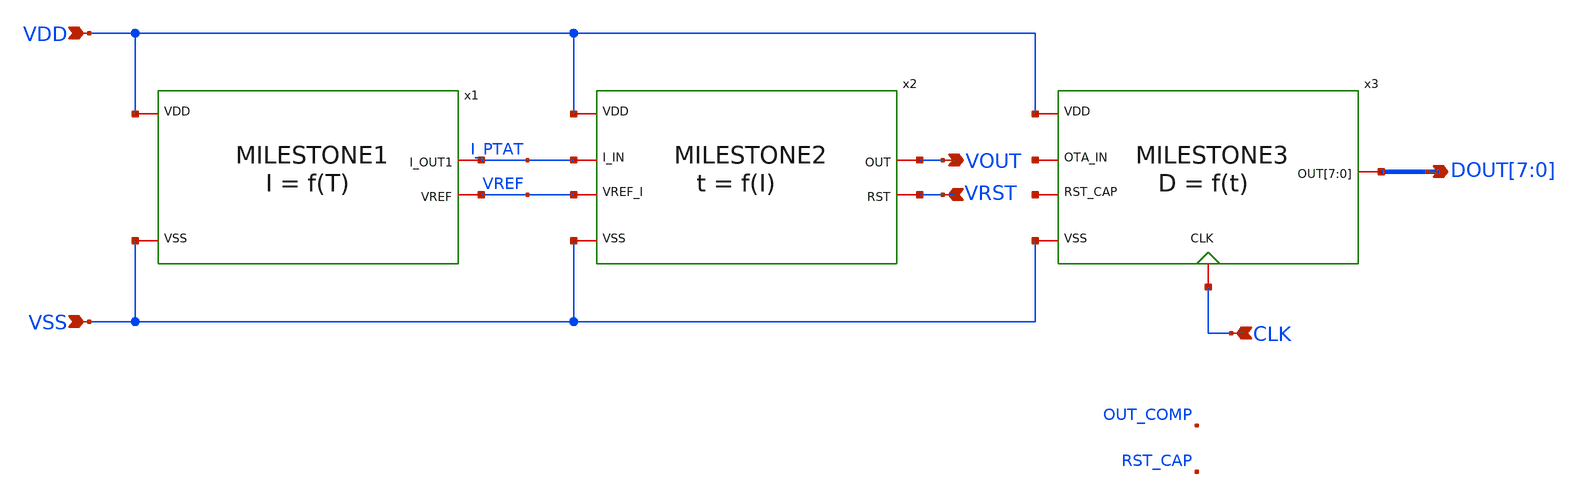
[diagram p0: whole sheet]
** sch_path: design/CNR_GR03_SKY130NM/TOPLEVEL.sch
**.subckt TOPLEVEL VDD VSS CLK DOUT[7],DOUT[6],DOUT[5],DOUT[4],DOUT[3],DOUT[2],DOUT[1],DOUT[0] VRST
*+ VOUT
*.ipin VDD
*.ipin VSS
*.ipin CLK
*.opin DOUT[7],DOUT[6],DOUT[5],DOUT[4],DOUT[3],DOUT[2],DOUT[1],DOUT[0]
*.ipin VRST
*.opin VOUT
x1 VDD I_PTAT VREF VSS MILESTONE1
x2 I_PTAT VREF VOUT VDD VRST VSS MILESTONE2
x3 net1 net2 CLK DOUT[7] DOUT[6] DOUT[5] DOUT[4] DOUT[3] DOUT[2] DOUT[1] DOUT[0] VDD VSS MILESTONE3
**.ends
.end
